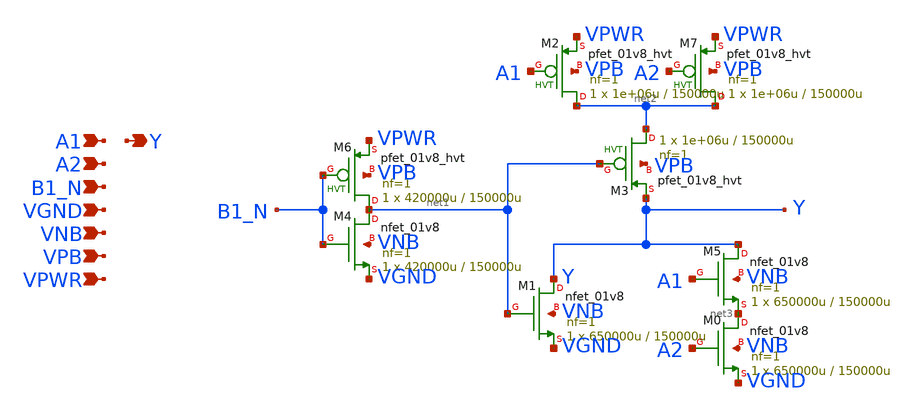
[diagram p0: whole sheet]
** sch_path: schematics/a21boi/sky130_fd_sc_hd__a21boi_1.sch
**.subckt sky130_fd_sc_hd__a21boi_1 A1 A2 B1_N VGND VNB VPB VPWR Y
*.ipin A1
*.ipin A2
*.ipin B1_N
*.ipin VGND
*.ipin VNB
*.ipin VPB
*.ipin VPWR
*.opin Y
XM6 net1 B1_N VPWR VPB sky130_fd_pr__pfet_01v8_hvt L=150000u W=420000u nf=1 ad='int((1 + 1)/2) * 420000u / 1 * 0.29'
+ as='int((1 + 2)/2) * 420000u / 1 * 0.29' pd='2*int((1 + 1)/2) * (420000u / 1 + 0.29)' ps='2*int((1 + 2)/2) * (420000u / 1 + 0.29)'
+ nrd='0.29 / 420000u ' nrs='0.29 / 420000u ' sa=0 sb=0 sd=0 mult=1 m=1
XM4 net1 B1_N VGND VNB sky130_fd_pr__nfet_01v8 L=150000u W=420000u nf=1 ad='int((1 + 1)/2) * 420000u / 1 * 0.29'
+ as='int((1 + 2)/2) * 420000u / 1 * 0.29' pd='2*int((1 + 1)/2) * (420000u / 1 + 0.29)' ps='2*int((1 + 2)/2) * (420000u / 1 + 0.29)'
+ nrd='0.29 / 420000u ' nrs='0.29 / 420000u ' sa=0 sb=0 sd=0 mult=1 m=1
XM2 net2 A1 VPWR VPB sky130_fd_pr__pfet_01v8_hvt L=150000u W=1e+06u nf=1 ad='int((1 + 1)/2) * 1e+06u / 1 * 0.29'
+ as='int((1 + 2)/2) * 1e+06u / 1 * 0.29' pd='2*int((1 + 1)/2) * (1e+06u / 1 + 0.29)' ps='2*int((1 + 2)/2) * (1e+06u / 1 + 0.29)'
+ nrd='0.29 / 1e+06u ' nrs='0.29 / 1e+06u ' sa=0 sb=0 sd=0 mult=1 m=1
XM7 net2 A2 VPWR VPB sky130_fd_pr__pfet_01v8_hvt L=150000u W=1e+06u nf=1 ad='int((1 + 1)/2) * 1e+06u / 1 * 0.29'
+ as='int((1 + 2)/2) * 1e+06u / 1 * 0.29' pd='2*int((1 + 1)/2) * (1e+06u / 1 + 0.29)' ps='2*int((1 + 2)/2) * (1e+06u / 1 + 0.29)'
+ nrd='0.29 / 1e+06u ' nrs='0.29 / 1e+06u ' sa=0 sb=0 sd=0 mult=1 m=1
XM3 net2 net1 Y VPB sky130_fd_pr__pfet_01v8_hvt L=150000u W=1e+06u nf=1 ad='int((1 + 1)/2) * 1e+06u / 1 * 0.29'
+ as='int((1 + 2)/2) * 1e+06u / 1 * 0.29' pd='2*int((1 + 1)/2) * (1e+06u / 1 + 0.29)' ps='2*int((1 + 2)/2) * (1e+06u / 1 + 0.29)'
+ nrd='0.29 / 1e+06u ' nrs='0.29 / 1e+06u ' sa=0 sb=0 sd=0 mult=1 m=1
XM5 Y A1 net3 VNB sky130_fd_pr__nfet_01v8 L=150000u W=650000u nf=1 ad='int((1 + 1)/2) * 650000u / 1 * 0.29'
+ as='int((1 + 2)/2) * 650000u / 1 * 0.29' pd='2*int((1 + 1)/2) * (650000u / 1 + 0.29)' ps='2*int((1 + 2)/2) * (650000u / 1 + 0.29)'
+ nrd='0.29 / 650000u ' nrs='0.29 / 650000u ' sa=0 sb=0 sd=0 mult=1 m=1
XM0 net3 A2 VGND VNB sky130_fd_pr__nfet_01v8 L=150000u W=650000u nf=1 ad='int((1 + 1)/2) * 650000u / 1 * 0.29'
+ as='int((1 + 2)/2) * 650000u / 1 * 0.29' pd='2*int((1 + 1)/2) * (650000u / 1 + 0.29)' ps='2*int((1 + 2)/2) * (650000u / 1 + 0.29)'
+ nrd='0.29 / 650000u ' nrs='0.29 / 650000u ' sa=0 sb=0 sd=0 mult=1 m=1
XM1 Y net1 VGND VNB sky130_fd_pr__nfet_01v8 L=150000u W=650000u nf=1 ad='int((1 + 1)/2) * 650000u / 1 * 0.29'
+ as='int((1 + 2)/2) * 650000u / 1 * 0.29' pd='2*int((1 + 1)/2) * (650000u / 1 + 0.29)' ps='2*int((1 + 2)/2) * (650000u / 1 + 0.29)'
+ nrd='0.29 / 650000u ' nrs='0.29 / 650000u ' sa=0 sb=0 sd=0 mult=1 m=1
**.ends
.end
